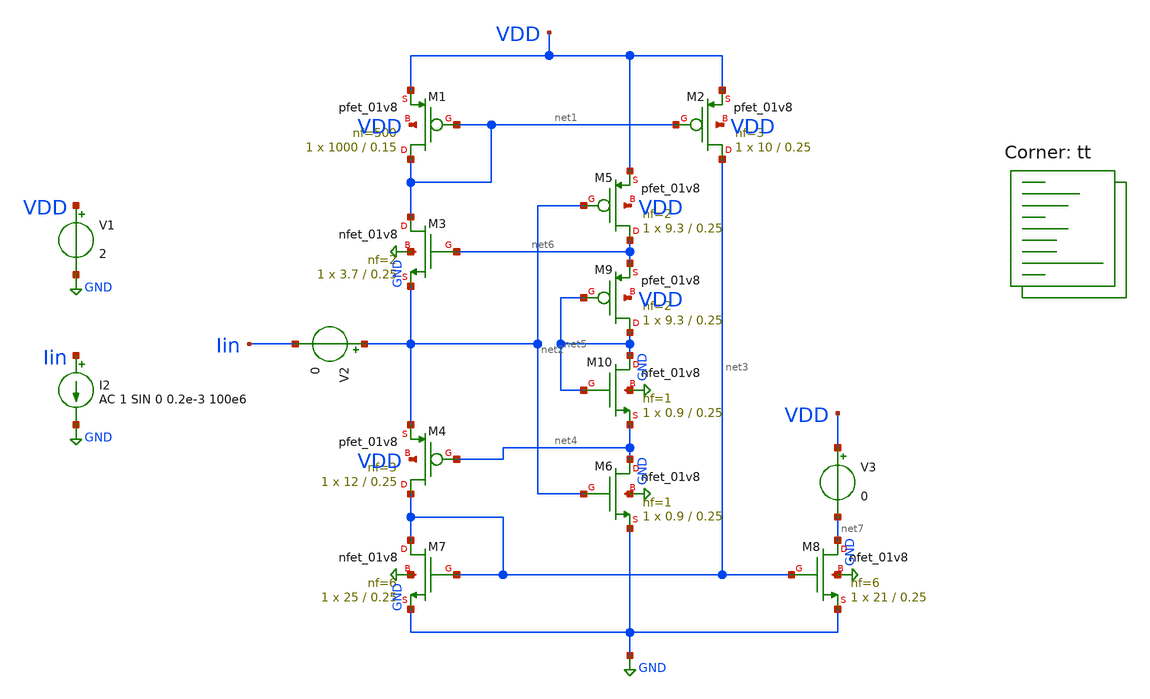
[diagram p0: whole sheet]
** sch_path: xschem/src/rectifier_hw.sch
**.subckt rectifier_hw
XM3 net1 net6 net2 GND sky130_fd_pr__nfet_01v8 L=0.25 W=3.7 nf=2 ad='int((nf+1)/2) * W/nf * 0.29' as='int((nf+2)/2) * W/nf * 0.29'
+ pd='2*int((nf+1)/2) * (W/nf + 0.29)' ps='2*int((nf+2)/2) * (W/nf + 0.29)' nrd='0.29 / W' nrs='0.29 / W'
+ sa=0 sb=0 sd=0 mult=1 m=1
XM1 net1 net1 VDD VDD sky130_fd_pr__pfet_01v8 L=0.15 W=1000 nf=500 ad='int((nf+1)/2) * W/nf * 0.29' as='int((nf+2)/2) * W/nf * 0.29'
+ pd='2*int((nf+1)/2) * (W/nf + 0.29)' ps='2*int((nf+2)/2) * (W/nf + 0.29)' nrd='0.29 / W' nrs='0.29 / W'
+ sa=0 sb=0 sd=0 mult=1 m=1
XM2 net3 net1 VDD VDD sky130_fd_pr__pfet_01v8 L=0.25 W=10 nf=3 ad='int((nf+1)/2) * W/nf * 0.29' as='int((nf+2)/2) * W/nf * 0.29'
+ pd='2*int((nf+1)/2) * (W/nf + 0.29)' ps='2*int((nf+2)/2) * (W/nf + 0.29)' nrd='0.29 / W' nrs='0.29 / W'
+ sa=0 sb=0 sd=0 mult=1 m=1
XM5 net6 net2 VDD VDD sky130_fd_pr__pfet_01v8 L=0.25 W=9.3 nf=2 ad='int((nf+1)/2) * W/nf * 0.29' as='int((nf+2)/2) * W/nf * 0.29'
+ pd='2*int((nf+1)/2) * (W/nf + 0.29)' ps='2*int((nf+2)/2) * (W/nf + 0.29)' nrd='0.29 / W' nrs='0.29 / W'
+ sa=0 sb=0 sd=0 mult=1 m=1
XM7 net3 net3 GND GND sky130_fd_pr__nfet_01v8 L=0.25 W=25 nf=6 ad='int((nf+1)/2) * W/nf * 0.29' as='int((nf+2)/2) * W/nf * 0.29'
+ pd='2*int((nf+1)/2) * (W/nf + 0.29)' ps='2*int((nf+2)/2) * (W/nf + 0.29)' nrd='0.29 / W' nrs='0.29 / W'
+ sa=0 sb=0 sd=0 mult=1 m=1
XM8 net7 net3 GND GND sky130_fd_pr__nfet_01v8 L=0.25 W=21 nf=6 ad='int((nf+1)/2) * W/nf * 0.29' as='int((nf+2)/2) * W/nf * 0.29'
+ pd='2*int((nf+1)/2) * (W/nf + 0.29)' ps='2*int((nf+2)/2) * (W/nf + 0.29)' nrd='0.29 / W' nrs='0.29 / W'
+ sa=0 sb=0 sd=0 mult=1 m=1
XM9 net5 net5 net6 VDD sky130_fd_pr__pfet_01v8 L=0.25 W=9.3 nf=2 ad='int((nf+1)/2) * W/nf * 0.29' as='int((nf+2)/2) * W/nf * 0.29'
+ pd='2*int((nf+1)/2) * (W/nf + 0.29)' ps='2*int((nf+2)/2) * (W/nf + 0.29)' nrd='0.29 / W' nrs='0.29 / W'
+ sa=0 sb=0 sd=0 mult=1 m=1
XM10 net5 net5 net4 GND sky130_fd_pr__nfet_01v8 L=0.25 W=0.9 nf=1 ad='int((nf+1)/2) * W/nf * 0.29' as='int((nf+2)/2) * W/nf * 0.29'
+ pd='2*int((nf+1)/2) * (W/nf + 0.29)' ps='2*int((nf+2)/2) * (W/nf + 0.29)' nrd='0.29 / W' nrs='0.29 / W'
+ sa=0 sb=0 sd=0 mult=1 m=1
XM4 net3 net4 net2 VDD sky130_fd_pr__pfet_01v8 L=0.25 W=12 nf=3 ad='int((nf+1)/2) * W/nf * 0.29' as='int((nf+2)/2) * W/nf * 0.29'
+ pd='2*int((nf+1)/2) * (W/nf + 0.29)' ps='2*int((nf+2)/2) * (W/nf + 0.29)' nrd='0.29 / W' nrs='0.29 / W'
+ sa=0 sb=0 sd=0 mult=1 m=1
XM6 net4 net2 GND GND sky130_fd_pr__nfet_01v8 L=0.25 W=0.9 nf=1 ad='int((nf+1)/2) * W/nf * 0.29' as='int((nf+2)/2) * W/nf * 0.29'
+ pd='2*int((nf+1)/2) * (W/nf + 0.29)' ps='2*int((nf+2)/2) * (W/nf + 0.29)' nrd='0.29 / W' nrs='0.29 / W'
+ sa=0 sb=0 sd=0 mult=1 m=1
V1 VDD GND 2
I2 Iin GND AC 1 SIN 0 0.2e-3 100e6
V3 VDD net7 0
V2 net2 Iin 0
**** begin user architecture code
.lib $::SKYWATER_MODELS/sky130.lib.spice tt



* ngspice commands
.options method=gear

.control
save all
ac dec 10 1 1e9
plot dB(v3#branch)
tran 1n .02u
plot v2#branch
plot v3#branch
.endc



**** end user architecture code
**.ends
.GLOBAL GND
.end
